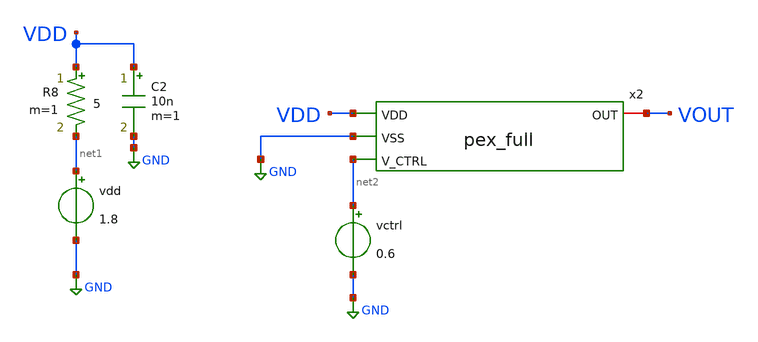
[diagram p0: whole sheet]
** sch_path: schem/temp_full_tb.sch
**.subckt temp_full_tb
vdd net1 GND 1.8
C2 VDD GND 10n m=1
R8 VDD net1 5 m=1
vctrl net2 GND 0.6
x2 VDD GND VOUT net2 vco_pex
**** begin user architecture code



.include /home/zhixuan/projects/fyp_vco/magic/full/vco_pex.spice
.lib /usr/local/share/pdk/sky130A/libs.tech/ngspice/sky130.lib.spice tt

.tran 0.1n 1u
.save all
.temp 50

.control
    run

    meas tran t11 when VOUT=0.9 rise=2
    meas tran t21 when VOUT=0.9 rise=3

    * Calculate period and frequency from 2nd period onwards
    let period = t21 - t11

    let freq = 1 / period

    print freq
.endc

.end


**** end user architecture code
**.ends
.GLOBAL GND
.end
